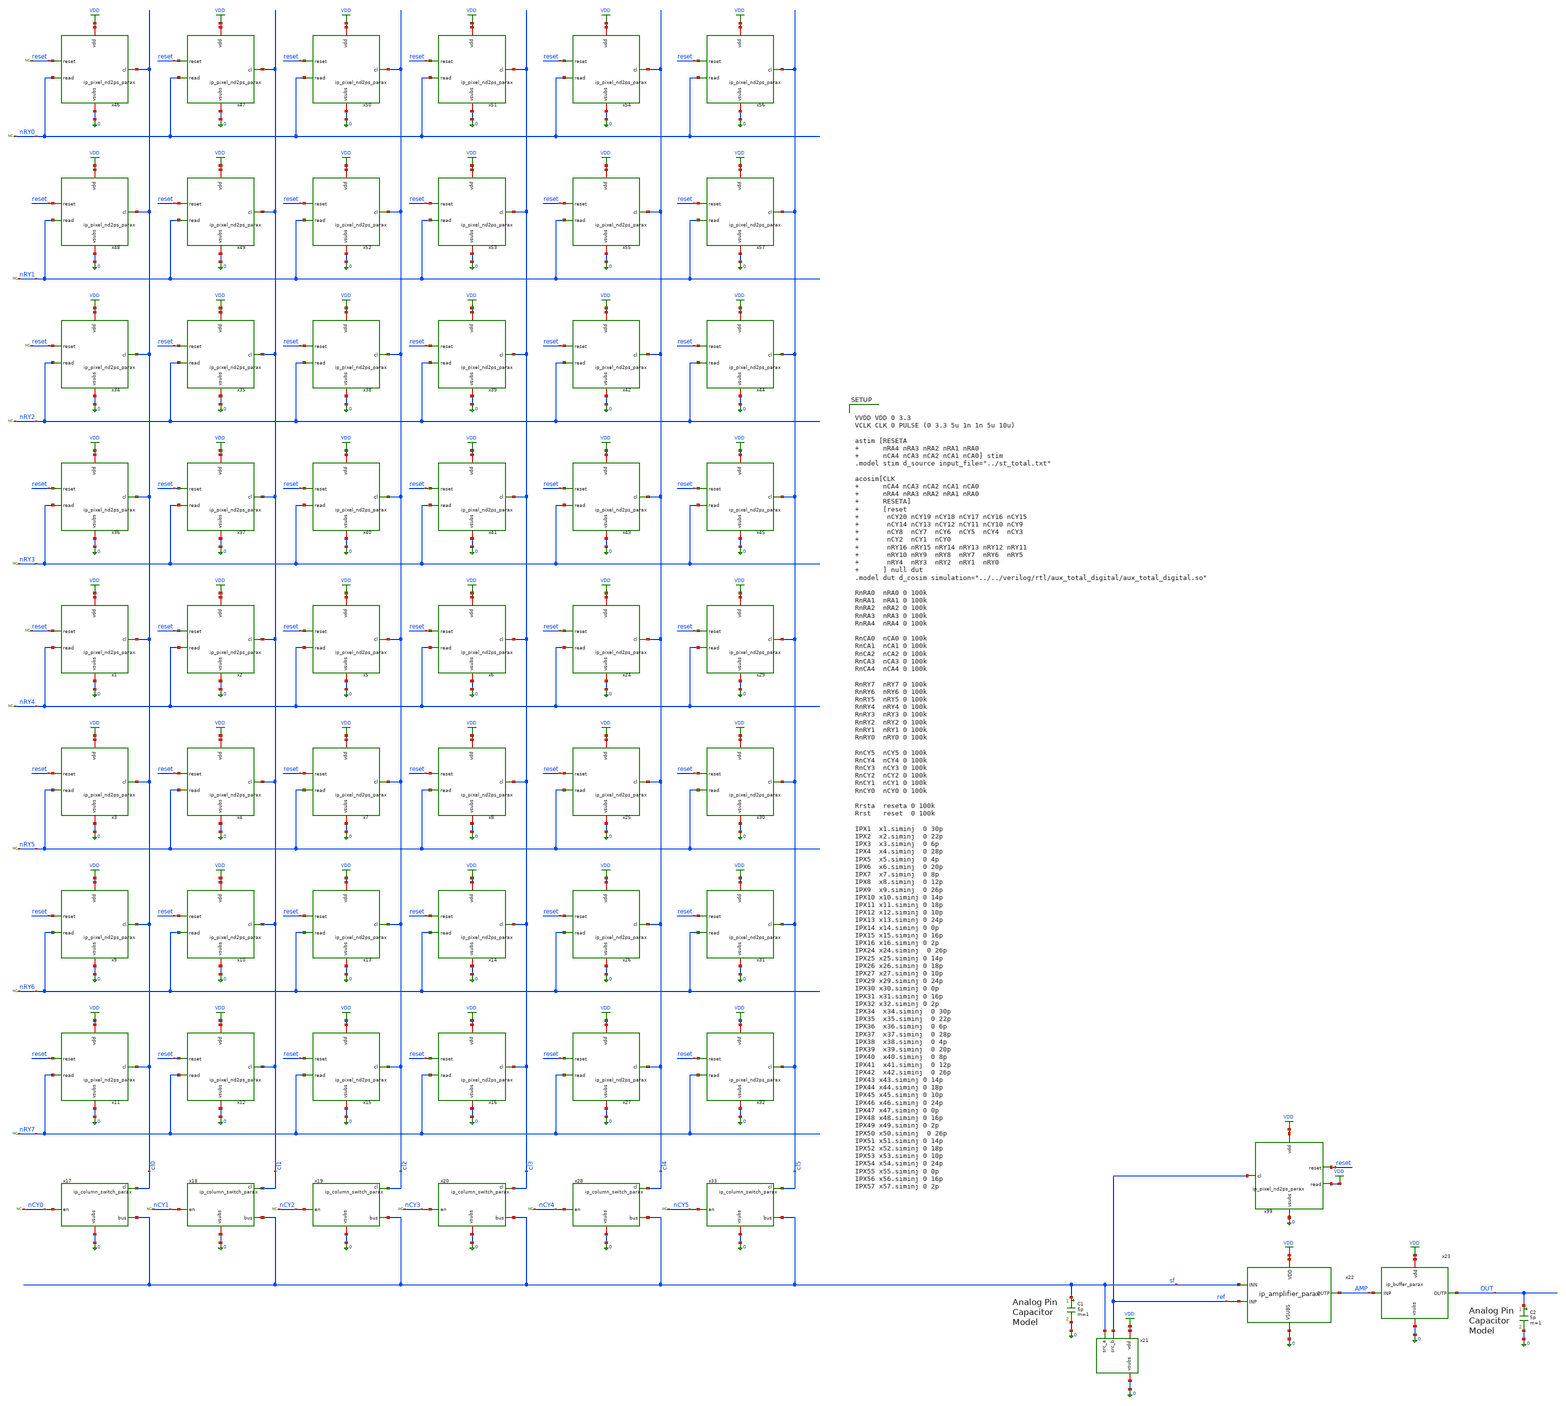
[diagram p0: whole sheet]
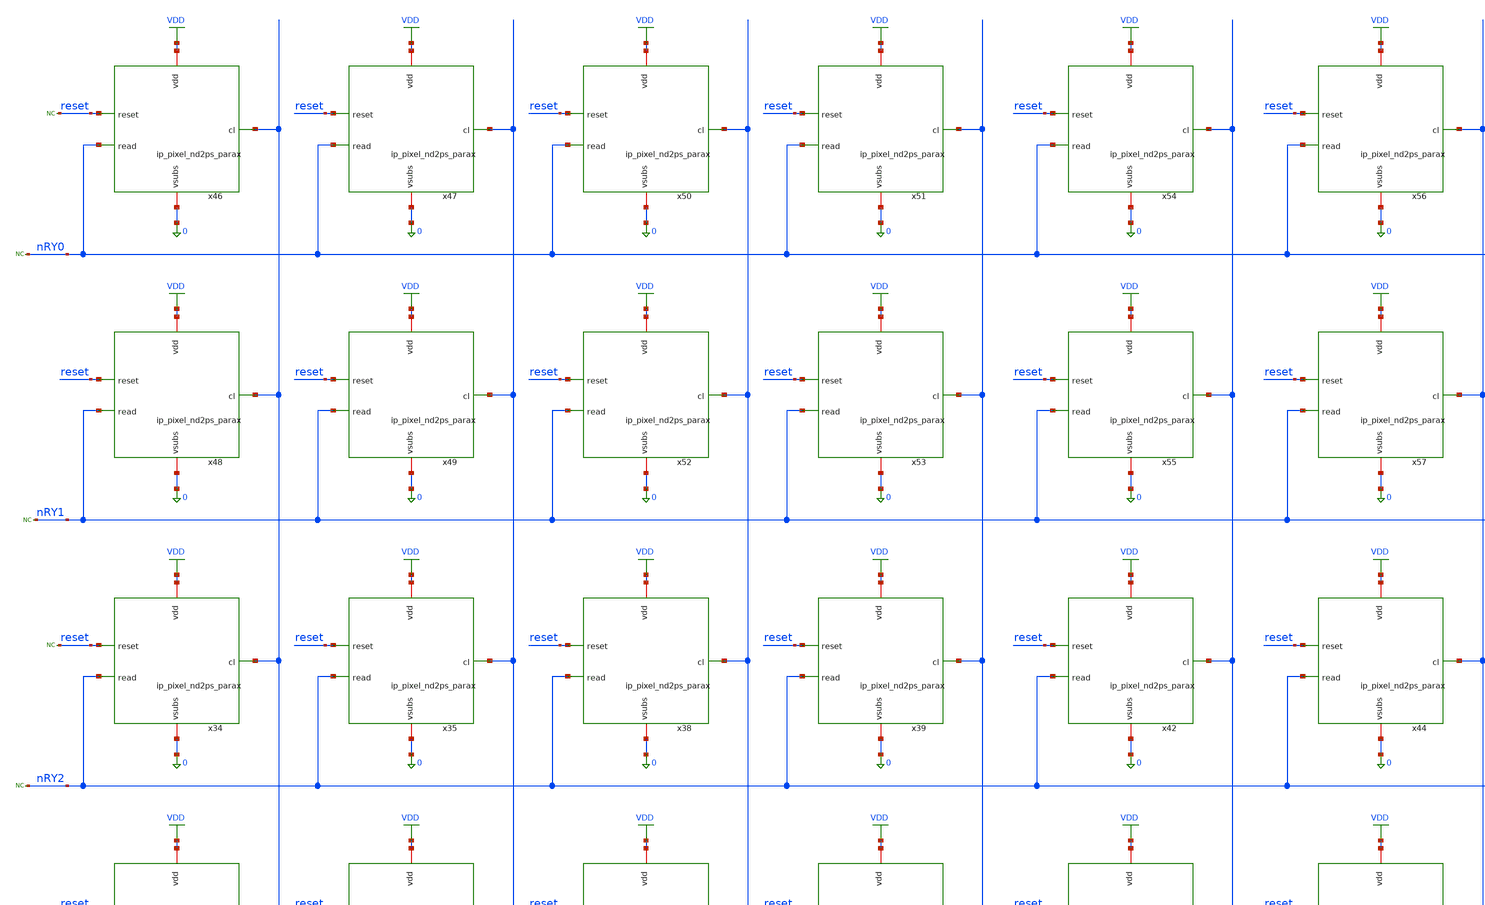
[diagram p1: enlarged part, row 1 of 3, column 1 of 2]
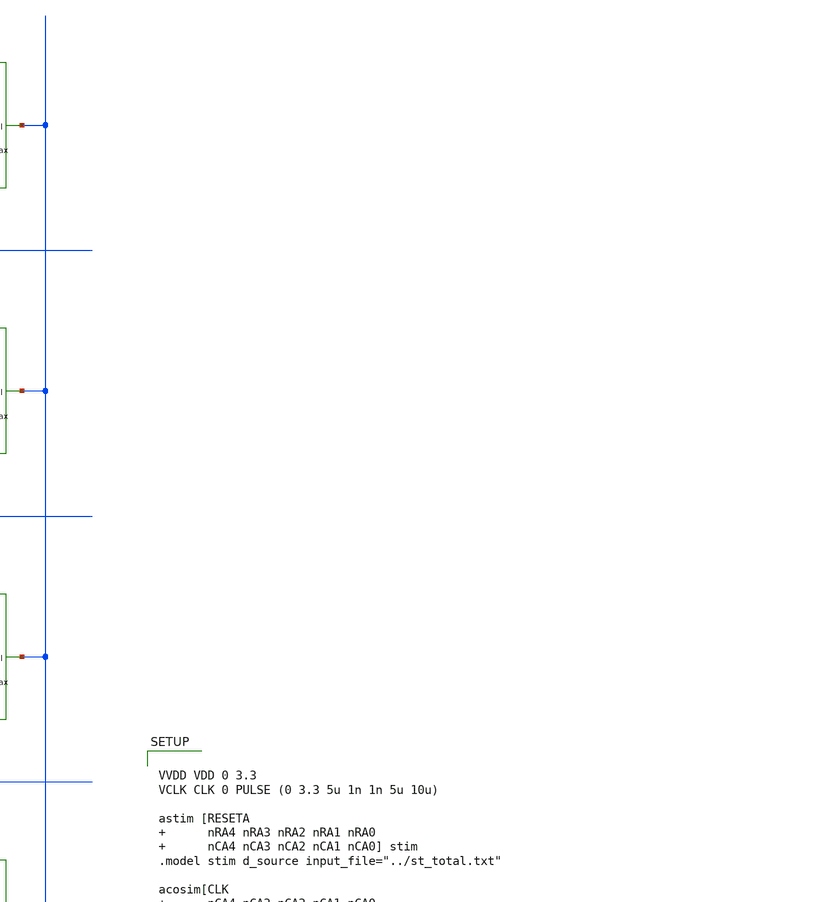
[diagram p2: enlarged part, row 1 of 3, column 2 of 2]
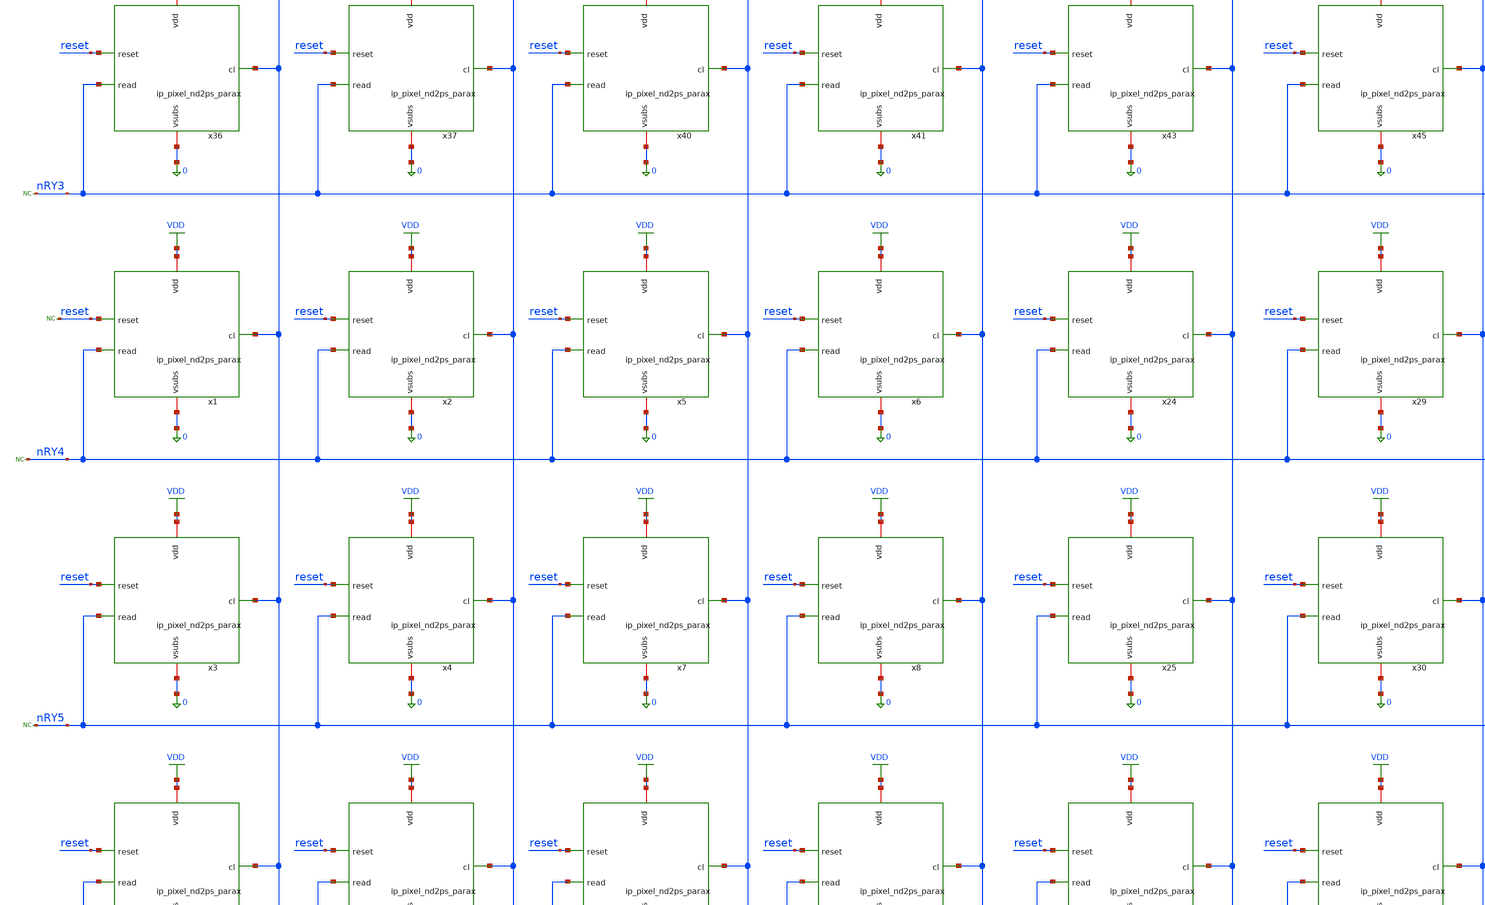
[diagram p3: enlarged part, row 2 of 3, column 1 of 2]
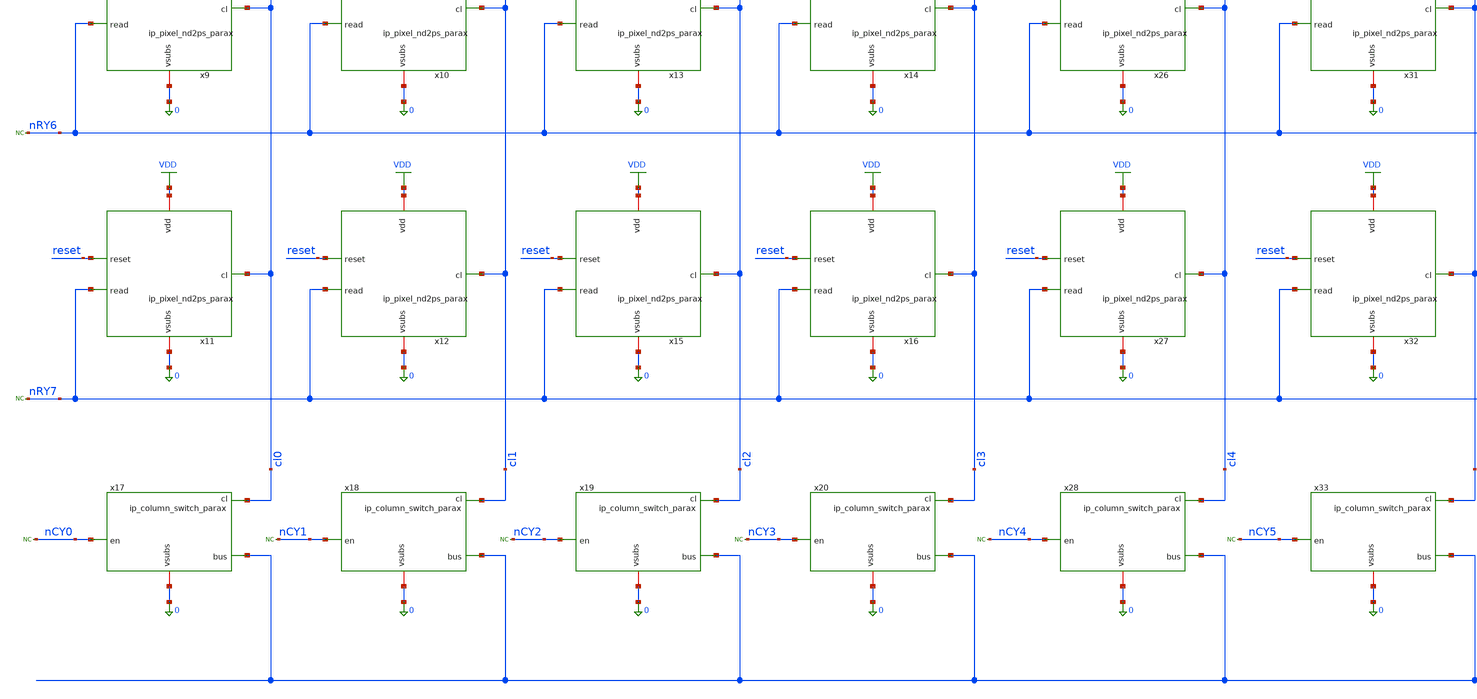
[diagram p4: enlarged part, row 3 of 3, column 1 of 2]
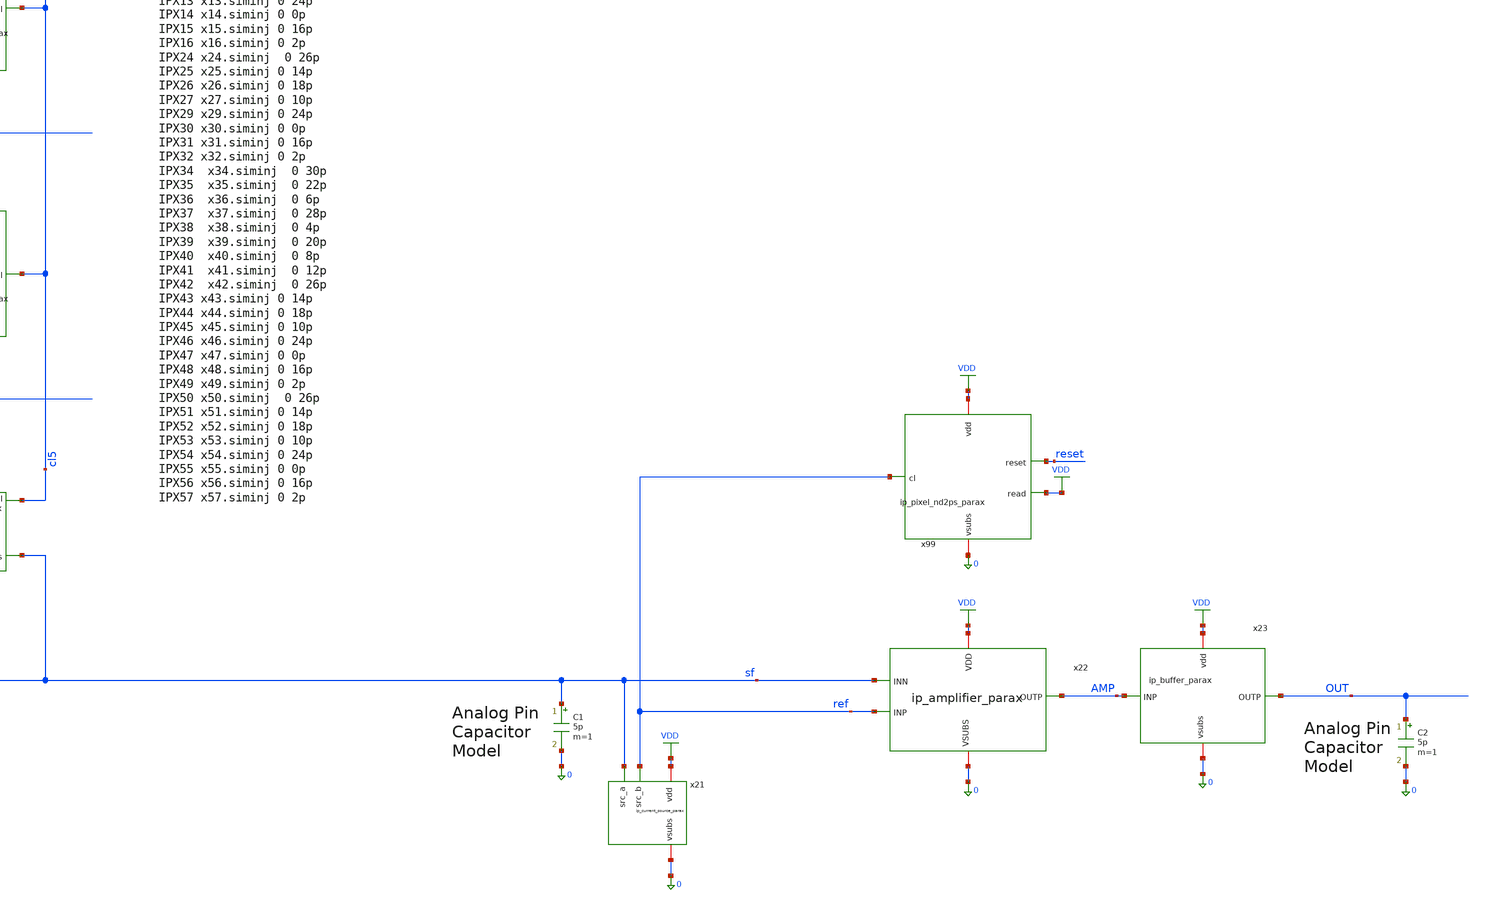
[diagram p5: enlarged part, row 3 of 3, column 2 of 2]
** sch_path: xschem/tb_total_tran.sch
**.subckt tb_total_tran
x1 VDD reset nRY4 0 cl0 ip_pixel_nd2ps_parax
x2 VDD reset nRY4 0 cl1 ip_pixel_nd2ps_parax
x3 VDD reset nRY5 0 cl0 ip_pixel_nd2ps_parax
x4 VDD reset nRY5 0 cl1 ip_pixel_nd2ps_parax
x5 VDD reset nRY4 0 cl2 ip_pixel_nd2ps_parax
x6 VDD reset nRY4 0 cl3 ip_pixel_nd2ps_parax
x7 VDD reset nRY5 0 cl2 ip_pixel_nd2ps_parax
x8 VDD reset nRY5 0 cl3 ip_pixel_nd2ps_parax
x9 VDD reset nRY6 0 cl0 ip_pixel_nd2ps_parax
x10 VDD reset nRY6 0 cl1 ip_pixel_nd2ps_parax
x11 VDD reset nRY7 0 cl0 ip_pixel_nd2ps_parax
x12 VDD reset nRY7 0 cl1 ip_pixel_nd2ps_parax
x13 VDD reset nRY6 0 cl2 ip_pixel_nd2ps_parax
x14 VDD reset nRY6 0 cl3 ip_pixel_nd2ps_parax
x15 VDD reset nRY7 0 cl2 ip_pixel_nd2ps_parax
x16 VDD reset nRY7 0 cl3 ip_pixel_nd2ps_parax
x17 cl0 sf nCY0 0 ip_column_switch_parax
x18 cl1 sf nCY1 0 ip_column_switch_parax
x19 cl2 sf nCY2 0 ip_column_switch_parax
x20 cl3 sf nCY3 0 ip_column_switch_parax
x21 VDD sf 0 ref ip_current_source_parax
x22 VDD AMP ref sf 0 ip_amplifier_parax
* noconn nRY4
* noconn nRY5
* noconn nRY6
* noconn nRY7
* noconn nCY0
* noconn nCY1
* noconn nCY2
* noconn nCY3
* noconn reset
x99 VDD reset VDD 0 ref ip_pixel_nd2ps_parax
C1 sf 0 5p m=1
x23 VDD OUT AMP 0 ip_buffer_parax
C2 OUT 0 5p m=1
x24 VDD reset nRY4 0 cl4 ip_pixel_nd2ps_parax
x25 VDD reset nRY5 0 cl4 ip_pixel_nd2ps_parax
x26 VDD reset nRY6 0 cl4 ip_pixel_nd2ps_parax
x27 VDD reset nRY7 0 cl4 ip_pixel_nd2ps_parax
x28 cl4 sf nCY4 0 ip_column_switch_parax
* noconn nCY4
x29 VDD reset nRY4 0 cl5 ip_pixel_nd2ps_parax
x30 VDD reset nRY5 0 cl5 ip_pixel_nd2ps_parax
x31 VDD reset nRY6 0 cl5 ip_pixel_nd2ps_parax
x32 VDD reset nRY7 0 cl5 ip_pixel_nd2ps_parax
x33 cl5 sf nCY5 0 ip_column_switch_parax
* noconn nCY5
x34 VDD reset nRY2 0 cl0 ip_pixel_nd2ps_parax
x35 VDD reset nRY2 0 cl1 ip_pixel_nd2ps_parax
x36 VDD reset nRY3 0 cl0 ip_pixel_nd2ps_parax
x37 VDD reset nRY3 0 cl1 ip_pixel_nd2ps_parax
x38 VDD reset nRY2 0 cl2 ip_pixel_nd2ps_parax
x39 VDD reset nRY2 0 cl3 ip_pixel_nd2ps_parax
x40 VDD reset nRY3 0 cl2 ip_pixel_nd2ps_parax
x41 VDD reset nRY3 0 cl3 ip_pixel_nd2ps_parax
* noconn nRY2
* noconn nRY3
* noconn reset
x42 VDD reset nRY2 0 cl4 ip_pixel_nd2ps_parax
x43 VDD reset nRY3 0 cl4 ip_pixel_nd2ps_parax
x44 VDD reset nRY2 0 cl5 ip_pixel_nd2ps_parax
x45 VDD reset nRY3 0 cl5 ip_pixel_nd2ps_parax
x46 VDD reset nRY0 0 cl0 ip_pixel_nd2ps_parax
x47 VDD reset nRY0 0 cl1 ip_pixel_nd2ps_parax
x48 VDD reset nRY1 0 cl0 ip_pixel_nd2ps_parax
x49 VDD reset nRY1 0 cl1 ip_pixel_nd2ps_parax
x50 VDD reset nRY0 0 cl2 ip_pixel_nd2ps_parax
x51 VDD reset nRY0 0 cl3 ip_pixel_nd2ps_parax
x52 VDD reset nRY1 0 cl2 ip_pixel_nd2ps_parax
x53 VDD reset nRY1 0 cl3 ip_pixel_nd2ps_parax
* noconn nRY0
* noconn nRY1
* noconn reset
x54 VDD reset nRY0 0 cl4 ip_pixel_nd2ps_parax
x55 VDD reset nRY1 0 cl4 ip_pixel_nd2ps_parax
x56 VDD reset nRY0 0 cl5 ip_pixel_nd2ps_parax
x57 VDD reset nRY1 0 cl5 ip_pixel_nd2ps_parax
**** begin user architecture code

.include $::180MCU_MODELS/design.ngspice
.lib $::180MCU_MODELS/sm141064.ngspice typical
.lib $::180MCU_MODELS/sm141064.ngspice res_typical
.lib $::180MCU_MODELS/sm141064.ngspice moscap_typical
.lib $::180MCU_MODELS/sm141064.ngspice diode_typical




.control
	reset
	tran 1u 1.8m
	save all
	write tb_total_tran.raw
	quit
.endc





VVDD VDD 0 3.3
VCLK CLK 0 PULSE (0 3.3 5u 1n 1n 5u 10u)

astim [RESETA        nRA4 nRA3 nRA2 nRA1 nRA0        nCA4 nCA3 nCA2 nCA1 nCA0] stim
.model stim d_source input_file="../st_total.txt"

acosim[CLK        nCA4 nCA3 nCA2 nCA1 nCA0        nRA4 nRA3 nRA2 nRA1 nRA0        RESETA]
+        [reset        nCY20 nCY19 nCY18 nCY17 nCY16 nCY15        nCY14 nCY13 nCY12 nCY11 nCY10 nCY9         nCY8
+  nCY7  nCY6  nCY5  nCY4  nCY3         nCY2  nCY1  nCY0         nRY16 nRY15 nRY14 nRY13 nRY12 nRY11
+         nRY10 nRY9  nRY8  nRY7  nRY6  nRY5        nRY4  nRY3  nRY2  nRY1  nRY0        ] null dut
.model dut d_cosim simulation="../../verilog/rtl/aux_total_digital/aux_total_digital.so"

RnRA0  nRA0 0 100k
RnRA1  nRA1 0 100k
RnRA2  nRA2 0 100k
RnRA3  nRA3 0 100k
RnRA4  nRA4 0 100k

RnCA0  nCA0 0 100k
RnCA1  nCA1 0 100k
RnCA2  nCA2 0 100k
RnCA3  nCA3 0 100k
RnCA4  nCA4 0 100k

RnRY7  nRY7 0 100k
RnRY6  nRY6 0 100k
RnRY5  nRY5 0 100k
RnRY4  nRY4 0 100k
RnRY3  nRY3 0 100k
RnRY2  nRY2 0 100k
RnRY1  nRY1 0 100k
RnRY0  nRY0 0 100k

RnCY5  nCY5 0 100k
RnCY4  nCY4 0 100k
RnCY3  nCY3 0 100k
RnCY2  nCY2 0 100k
RnCY1  nCY1 0 100k
RnCY0  nCY0 0 100k

Rrsta  reseta 0 100k
Rrst   reset  0 100k

IPX1  x1.siminj  0 30p
IPX2  x2.siminj  0 22p
IPX3  x3.siminj  0 6p
IPX4  x4.siminj  0 28p
IPX5  x5.siminj  0 4p
IPX6  x6.siminj  0 20p
IPX7  x7.siminj  0 8p
IPX8  x8.siminj  0 12p
IPX9  x9.siminj  0 26p
IPX10 x10.siminj 0 14p
IPX11 x11.siminj 0 18p
IPX12 x12.siminj 0 10p
IPX13 x13.siminj 0 24p
IPX14 x14.siminj 0 0p
IPX15 x15.siminj 0 16p
IPX16 x16.siminj 0 2p
IPX24 x24.siminj  0 26p
IPX25 x25.siminj 0 14p
IPX26 x26.siminj 0 18p
IPX27 x27.siminj 0 10p
IPX29 x29.siminj 0 24p
IPX30 x30.siminj 0 0p
IPX31 x31.siminj 0 16p
IPX32 x32.siminj 0 2p
IPX34  x34.siminj  0 30p
IPX35  x35.siminj  0 22p
IPX36  x36.siminj  0 6p
IPX37  x37.siminj  0 28p
IPX38  x38.siminj  0 4p
IPX39  x39.siminj  0 20p
IPX40  x40.siminj  0 8p
IPX41  x41.siminj  0 12p
IPX42  x42.siminj  0 26p
IPX43 x43.siminj 0 14p
IPX44 x44.siminj 0 18p
IPX45 x45.siminj 0 10p
IPX46 x46.siminj 0 24p
IPX47 x47.siminj 0 0p
IPX48 x48.siminj 0 16p
IPX49 x49.siminj 0 2p
IPX50 x50.siminj  0 26p
IPX51 x51.siminj 0 14p
IPX52 x52.siminj 0 18p
IPX53 x53.siminj 0 10p
IPX54 x54.siminj 0 24p
IPX55 x55.siminj 0 0p
IPX56 x56.siminj 0 16p
IPX57 x57.siminj 0 2p


**** end user architecture code
**.ends

* expanding   symbol:  ip_pixel_nd2ps_parax.sym # of pins=5
** sym_path: xschem/ip_pixel_nd2ps.sym
.include [file normalize ./parax/ip_pixel_nd2ps.sim.spice]

* expanding   symbol:  ip_column_switch_parax.sym # of pins=4
** sym_path: xschem/ip_column_switch.sym
.include [file normalize ./parax/ip_column_switch.sim.spice]

* expanding   symbol:  ip_current_source_parax.sym # of pins=4
** sym_path: xschem/ip_current_source.sym
.include [file normalize ./parax/ip_current_source.sim.spice]

* expanding   symbol:  ip_amplifier_parax.sym # of pins=5
** sym_path: xschem/ip_amplifier.sym
.include [file normalize ./parax/ip_amplifier.sim.spice]

* expanding   symbol:  ip_buffer_parax.sym # of pins=4
** sym_path: xschem/ip_buffer.sym
.include [file normalize ./parax/ip_buffer.sim.spice]
.GLOBAL VDD
.end
